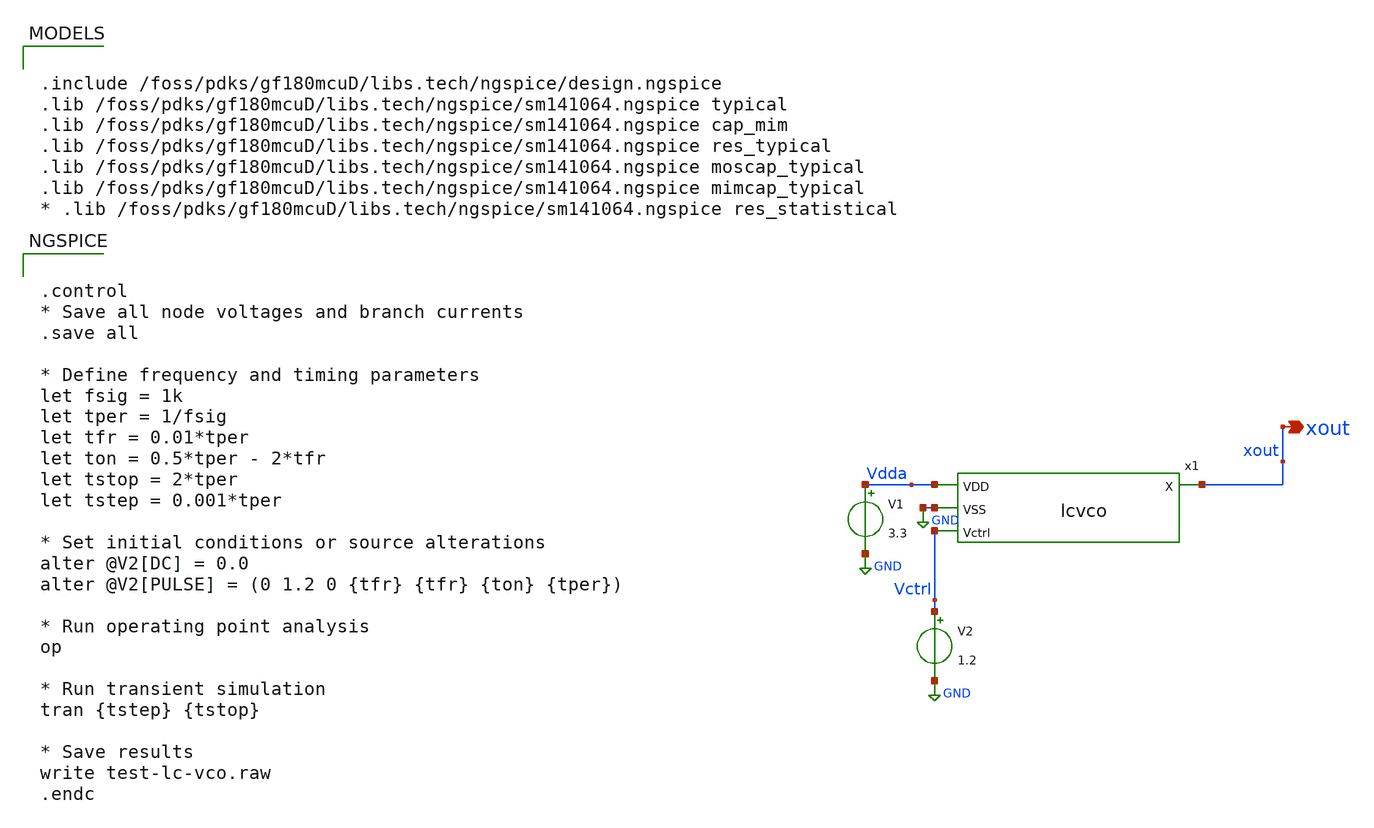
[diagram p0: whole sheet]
** sch_path: Project/1-on-chip/schematic/VCO/lc-vco/test-lc-vco.sch
**.subckt test-lc-vco xout
*.opin xout
V1 Vdda GND 3.3
V2 Vctrl GND 1.2
x1 Vdda xout GND Vctrl lcvco
**** begin user architecture code

.include /foss/pdks/gf180mcuD/libs.tech/ngspice/design.ngspice
.lib /foss/pdks/gf180mcuD/libs.tech/ngspice/sm141064.ngspice typical
.lib /foss/pdks/gf180mcuD/libs.tech/ngspice/sm141064.ngspice cap_mim
.lib /foss/pdks/gf180mcuD/libs.tech/ngspice/sm141064.ngspice res_typical
.lib /foss/pdks/gf180mcuD/libs.tech/ngspice/sm141064.ngspice moscap_typical
.lib /foss/pdks/gf180mcuD/libs.tech/ngspice/sm141064.ngspice mimcap_typical
* .lib /foss/pdks/gf180mcuD/libs.tech/ngspice/sm141064.ngspice res_statistical



.control
* Save all node voltages and branch currents
.save all

* Define frequency and timing parameters
let fsig = 1k
let tper = 1/fsig
let tfr = 0.01*tper
let ton = 0.5*tper - 2*tfr
let tstop = 2*tper
let tstep = 0.001*tper

* Set initial conditions or source alterations
alter @V2[DC] = 0.0
alter @V2[PULSE] = (0 1.2 0 {tfr} {tfr} {ton} {tper})

* Run operating point analysis
op

* Run transient simulation
tran {tstep} {tstop}

* Save results
write test-lc-vco.raw
.endc



**** end user architecture code
**.ends
.GLOBAL GND
.end
